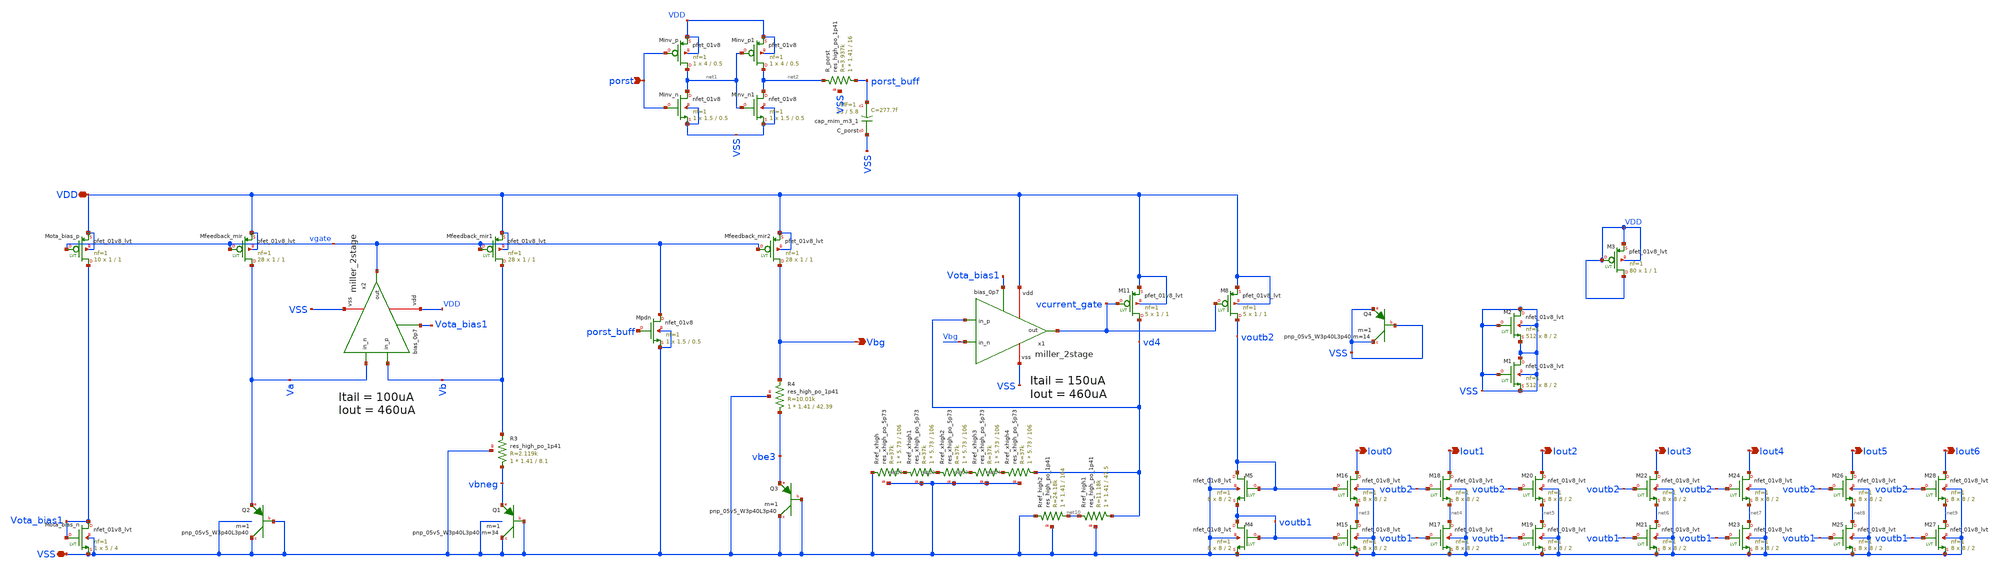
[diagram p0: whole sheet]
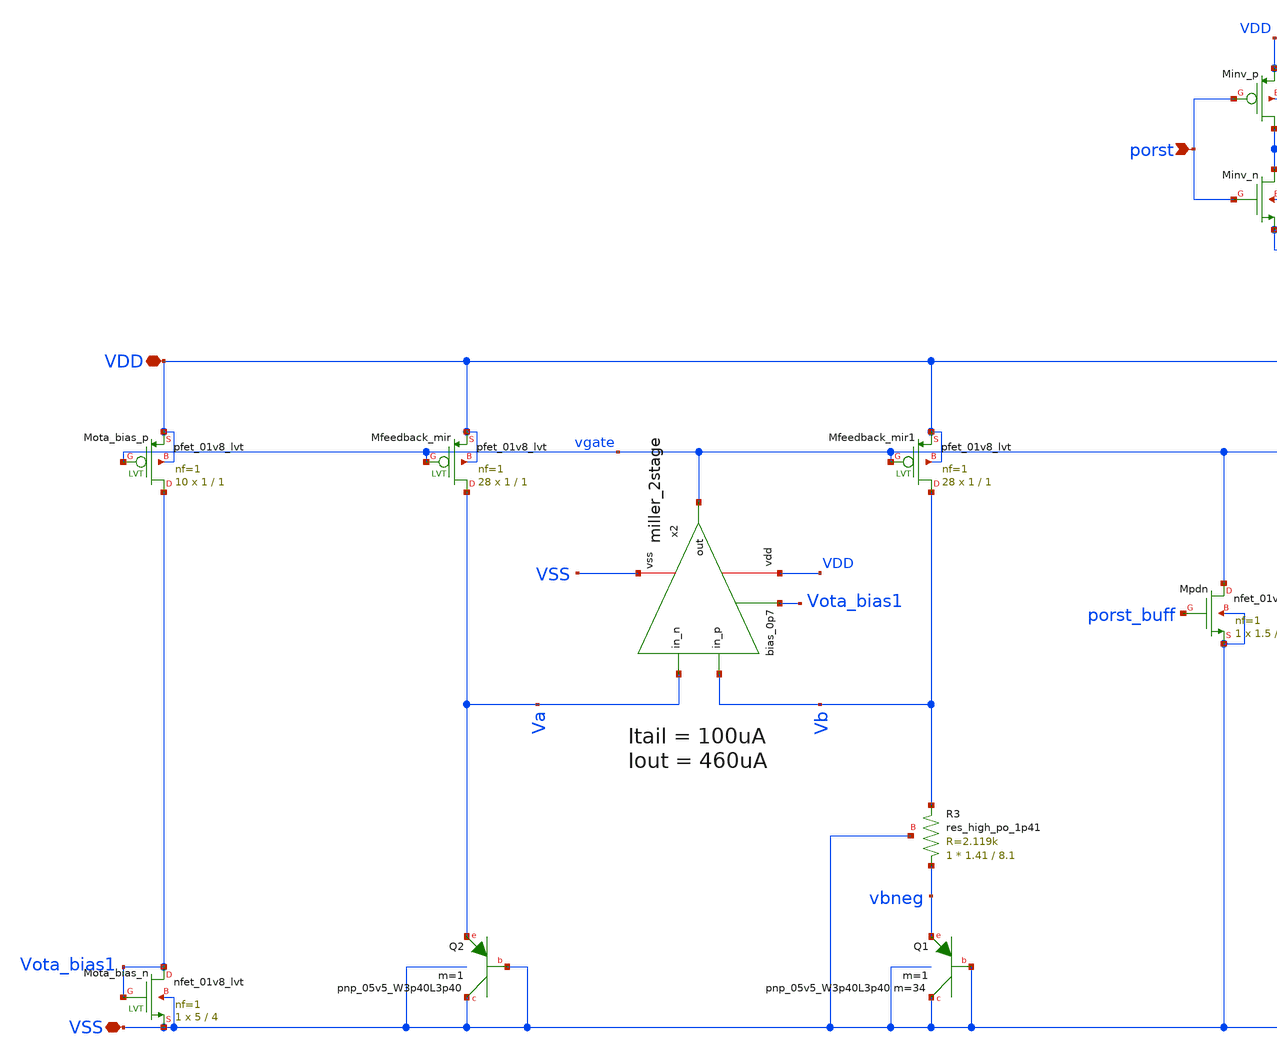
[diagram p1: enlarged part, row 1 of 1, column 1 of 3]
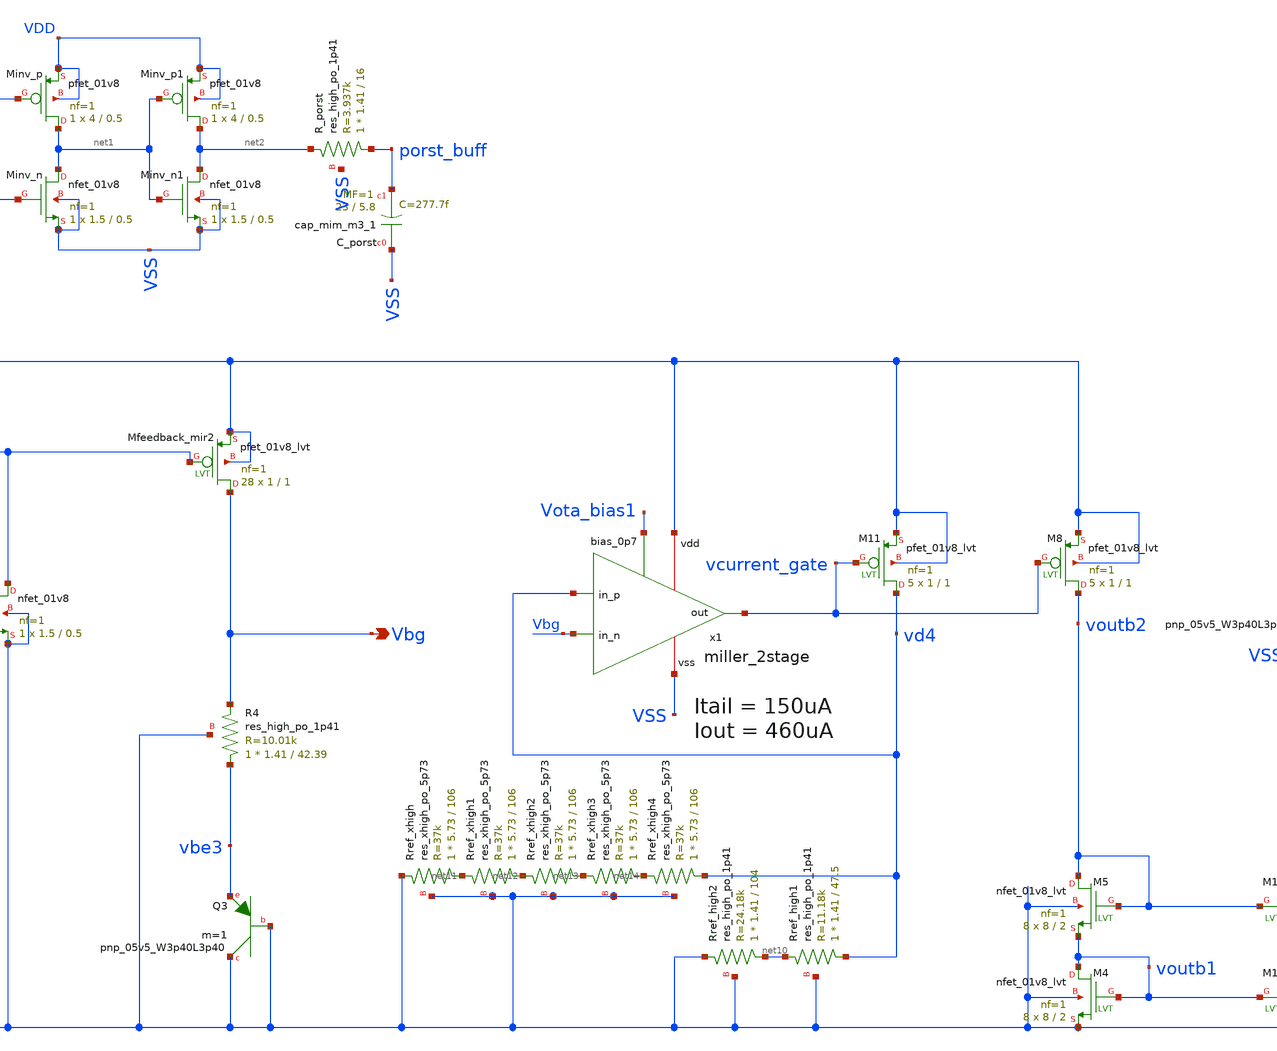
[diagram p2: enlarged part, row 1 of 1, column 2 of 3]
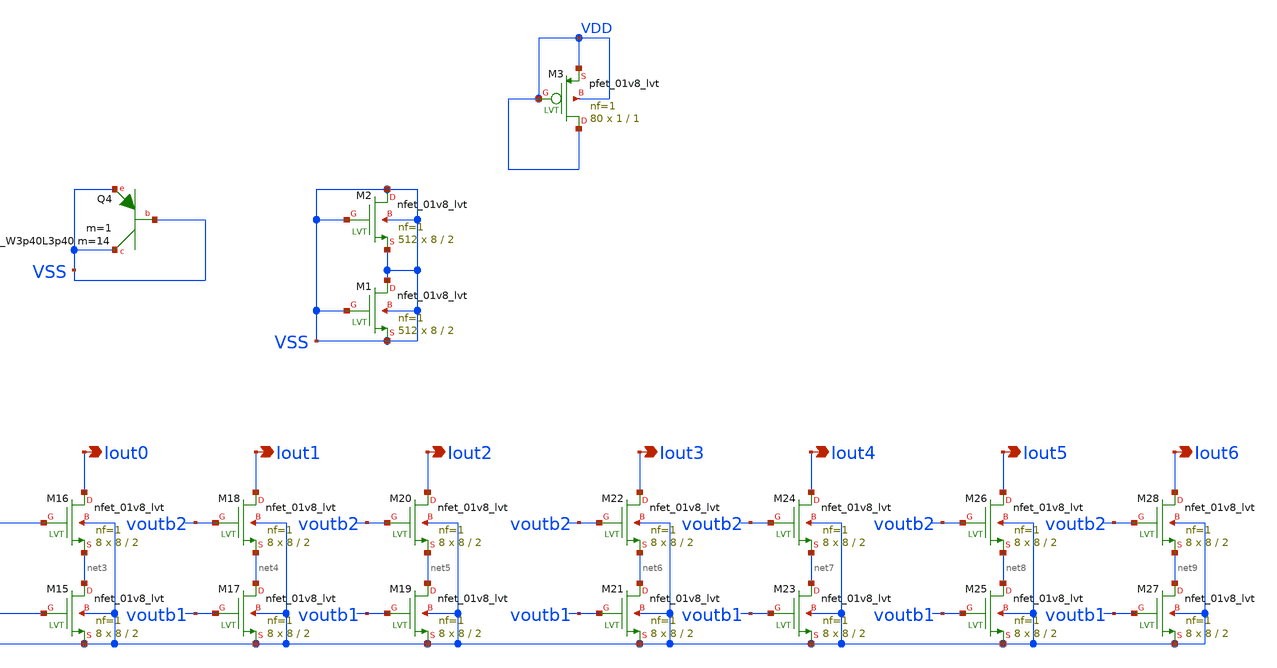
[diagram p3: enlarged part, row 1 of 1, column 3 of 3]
** sch_path: xschem/current_reference/BGR_lvs.sch
**.subckt BGR_lvs Iout0 VDD VSS Iout1 Iout2 porst Vbg Iout3 Iout4 Iout5 Iout6
*.opin Iout0
*.iopin VDD
*.iopin VSS
*.opin Iout1
*.opin Iout2
*.ipin porst
*.opin Vbg
*.opin Iout3
*.opin Iout4
*.opin Iout5
*.opin Iout6
XQ2 VSS VSS Va sky130_fd_pr__pnp_05v5_W3p40L3p40 m=1
XQ1 VSS VSS vbneg sky130_fd_pr__pnp_05v5_W3p40L3p40 m=34 m=1
XMota_bias_n Vota_bias1 Vota_bias1 VSS VSS sky130_fd_pr__nfet_01v8_lvt L=4 W=5 nf=1 ad='int((nf+1)/2) * W/nf * 0.29'
+ as='int((nf+2)/2) * W/nf * 0.29' pd='2*int((nf+1)/2) * (W/nf + 0.29)' ps='2*int((nf+2)/2) * (W/nf + 0.29)'
+ nrd='0.29 / W' nrs='0.29 / W' sa=0 sb=0 sd=0 mult=1 m=1
XMota_bias_p Vota_bias1 vgate VDD VDD sky130_fd_pr__pfet_01v8_lvt L=1 W=1 nf=1 ad='int((nf+1)/2) * W/nf * 0.29'
+ as='int((nf+2)/2) * W/nf * 0.29' pd='2*int((nf+1)/2) * (W/nf + 0.29)' ps='2*int((nf+2)/2) * (W/nf + 0.29)'
+ nrd='0.29 / W' nrs='0.29 / W' sa=0 sb=0 sd=0 mult=10 m=10
XMfeedback_mir Va vgate VDD VDD sky130_fd_pr__pfet_01v8_lvt L=1 W=1 nf=1 ad='int((nf+1)/2) * W/nf * 0.29'
+ as='int((nf+2)/2) * W/nf * 0.29' pd='2*int((nf+1)/2) * (W/nf + 0.29)' ps='2*int((nf+2)/2) * (W/nf + 0.29)'
+ nrd='0.29 / W' nrs='0.29 / W' sa=0 sb=0 sd=0 mult=28 m=28
XMfeedback_mir1 Vb vgate VDD VDD sky130_fd_pr__pfet_01v8_lvt L=1 W=1 nf=1 ad='int((nf+1)/2) * W/nf * 0.29'
+ as='int((nf+2)/2) * W/nf * 0.29' pd='2*int((nf+1)/2) * (W/nf + 0.29)' ps='2*int((nf+2)/2) * (W/nf + 0.29)'
+ nrd='0.29 / W' nrs='0.29 / W' sa=0 sb=0 sd=0 mult=28 m=28
XMfeedback_mir2 Vbg vgate VDD VDD sky130_fd_pr__pfet_01v8_lvt L=1 W=1 nf=1 ad='int((nf+1)/2) * W/nf * 0.29'
+ as='int((nf+2)/2) * W/nf * 0.29' pd='2*int((nf+1)/2) * (W/nf + 0.29)' ps='2*int((nf+2)/2) * (W/nf + 0.29)'
+ nrd='0.29 / W' nrs='0.29 / W' sa=0 sb=0 sd=0 mult=28 m=28
XQ3 VSS VSS vbe3 sky130_fd_pr__pnp_05v5_W3p40L3p40 m=1
XM11 vd4 vcurrent_gate VDD VDD sky130_fd_pr__pfet_01v8_lvt L=1 W=1 nf=1 ad='int((nf+1)/2) * W/nf * 0.29'
+ as='int((nf+2)/2) * W/nf * 0.29' pd='2*int((nf+1)/2) * (W/nf + 0.29)' ps='2*int((nf+2)/2) * (W/nf + 0.29)'
+ nrd='0.29 / W' nrs='0.29 / W' sa=0 sb=0 sd=0 mult=5 m=5
XM8 voutb2 vcurrent_gate VDD VDD sky130_fd_pr__pfet_01v8_lvt L=1 W=1 nf=1 ad='int((nf+1)/2) * W/nf * 0.29'
+ as='int((nf+2)/2) * W/nf * 0.29' pd='2*int((nf+1)/2) * (W/nf + 0.29)' ps='2*int((nf+2)/2) * (W/nf + 0.29)'
+ nrd='0.29 / W' nrs='0.29 / W' sa=0 sb=0 sd=0 mult=5 m=5
XM4 voutb1 voutb1 VSS VSS sky130_fd_pr__nfet_01v8_lvt L=2 W=8 nf=1 ad='int((nf+1)/2) * W/nf * 0.29' as='int((nf+2)/2) * W/nf * 0.29'
+ pd='2*int((nf+1)/2) * (W/nf + 0.29)' ps='2*int((nf+2)/2) * (W/nf + 0.29)' nrd='0.29 / W' nrs='0.29 / W'
+ sa=0 sb=0 sd=0 mult=8 m=8
XM5 voutb2 voutb2 voutb1 VSS sky130_fd_pr__nfet_01v8_lvt L=2 W=8 nf=1 ad='int((nf+1)/2) * W/nf * 0.29'
+ as='int((nf+2)/2) * W/nf * 0.29' pd='2*int((nf+1)/2) * (W/nf + 0.29)' ps='2*int((nf+2)/2) * (W/nf + 0.29)'
+ nrd='0.29 / W' nrs='0.29 / W' sa=0 sb=0 sd=0 mult=8 m=8
XMinv_n net1 porst VSS VSS sky130_fd_pr__nfet_01v8 L=0.5 W=1.5 nf=1 ad='int((nf+1)/2) * W/nf * 0.29'
+ as='int((nf+2)/2) * W/nf * 0.29' pd='2*int((nf+1)/2) * (W/nf + 0.29)' ps='2*int((nf+2)/2) * (W/nf + 0.29)'
+ nrd='0.29 / W' nrs='0.29 / W' sa=0 sb=0 sd=0 mult=1 m=1
XMinv_p net1 porst VDD VDD sky130_fd_pr__pfet_01v8 L=0.5 W=4 nf=1 ad='int((nf+1)/2) * W/nf * 0.29' as='int((nf+2)/2) * W/nf * 0.29'
+ pd='2*int((nf+1)/2) * (W/nf + 0.29)' ps='2*int((nf+2)/2) * (W/nf + 0.29)' nrd='0.29 / W' nrs='0.29 / W'
+ sa=0 sb=0 sd=0 mult=1 m=1
XMinv_n1 net2 net1 VSS VSS sky130_fd_pr__nfet_01v8 L=0.5 W=1.5 nf=1 ad='int((nf+1)/2) * W/nf * 0.29'
+ as='int((nf+2)/2) * W/nf * 0.29' pd='2*int((nf+1)/2) * (W/nf + 0.29)' ps='2*int((nf+2)/2) * (W/nf + 0.29)'
+ nrd='0.29 / W' nrs='0.29 / W' sa=0 sb=0 sd=0 mult=1 m=1
XMinv_p1 net2 net1 VDD VDD sky130_fd_pr__pfet_01v8 L=0.5 W=4 nf=1 ad='int((nf+1)/2) * W/nf * 0.29' as='int((nf+2)/2) * W/nf * 0.29'
+ pd='2*int((nf+1)/2) * (W/nf + 0.29)' ps='2*int((nf+2)/2) * (W/nf + 0.29)' nrd='0.29 / W' nrs='0.29 / W'
+ sa=0 sb=0 sd=0 mult=1 m=1
XM15 net3 voutb1 VSS VSS sky130_fd_pr__nfet_01v8_lvt L=2 W=8 nf=1 ad='int((nf+1)/2) * W/nf * 0.29' as='int((nf+2)/2) * W/nf * 0.29'
+ pd='2*int((nf+1)/2) * (W/nf + 0.29)' ps='2*int((nf+2)/2) * (W/nf + 0.29)' nrd='0.29 / W' nrs='0.29 / W'
+ sa=0 sb=0 sd=0 mult=8 m=8
XM16 Iout0 voutb2 net3 VSS sky130_fd_pr__nfet_01v8_lvt L=2 W=8 nf=1 ad='int((nf+1)/2) * W/nf * 0.29'
+ as='int((nf+2)/2) * W/nf * 0.29' pd='2*int((nf+1)/2) * (W/nf + 0.29)' ps='2*int((nf+2)/2) * (W/nf + 0.29)'
+ nrd='0.29 / W' nrs='0.29 / W' sa=0 sb=0 sd=0 mult=8 m=8
XM17 net4 voutb1 VSS VSS sky130_fd_pr__nfet_01v8_lvt L=2 W=8 nf=1 ad='int((nf+1)/2) * W/nf * 0.29' as='int((nf+2)/2) * W/nf * 0.29'
+ pd='2*int((nf+1)/2) * (W/nf + 0.29)' ps='2*int((nf+2)/2) * (W/nf + 0.29)' nrd='0.29 / W' nrs='0.29 / W'
+ sa=0 sb=0 sd=0 mult=8 m=8
XM18 Iout1 voutb2 net4 VSS sky130_fd_pr__nfet_01v8_lvt L=2 W=8 nf=1 ad='int((nf+1)/2) * W/nf * 0.29'
+ as='int((nf+2)/2) * W/nf * 0.29' pd='2*int((nf+1)/2) * (W/nf + 0.29)' ps='2*int((nf+2)/2) * (W/nf + 0.29)'
+ nrd='0.29 / W' nrs='0.29 / W' sa=0 sb=0 sd=0 mult=8 m=8
XC_porst VSS porst_buff sky130_fd_pr__cap_mim_m3_1 W=23 L=5.8 MF=1 m=1
XM19 net5 voutb1 VSS VSS sky130_fd_pr__nfet_01v8_lvt L=2 W=8 nf=1 ad='int((nf+1)/2) * W/nf * 0.29' as='int((nf+2)/2) * W/nf * 0.29'
+ pd='2*int((nf+1)/2) * (W/nf + 0.29)' ps='2*int((nf+2)/2) * (W/nf + 0.29)' nrd='0.29 / W' nrs='0.29 / W'
+ sa=0 sb=0 sd=0 mult=8 m=8
XM20 Iout2 voutb2 net5 VSS sky130_fd_pr__nfet_01v8_lvt L=2 W=8 nf=1 ad='int((nf+1)/2) * W/nf * 0.29'
+ as='int((nf+2)/2) * W/nf * 0.29' pd='2*int((nf+1)/2) * (W/nf + 0.29)' ps='2*int((nf+2)/2) * (W/nf + 0.29)'
+ nrd='0.29 / W' nrs='0.29 / W' sa=0 sb=0 sd=0 mult=8 m=8
XM21 net6 voutb1 VSS VSS sky130_fd_pr__nfet_01v8_lvt L=2 W=8 nf=1 ad='int((nf+1)/2) * W/nf * 0.29' as='int((nf+2)/2) * W/nf * 0.29'
+ pd='2*int((nf+1)/2) * (W/nf + 0.29)' ps='2*int((nf+2)/2) * (W/nf + 0.29)' nrd='0.29 / W' nrs='0.29 / W'
+ sa=0 sb=0 sd=0 mult=8 m=8
XM22 Iout3 voutb2 net6 VSS sky130_fd_pr__nfet_01v8_lvt L=2 W=8 nf=1 ad='int((nf+1)/2) * W/nf * 0.29'
+ as='int((nf+2)/2) * W/nf * 0.29' pd='2*int((nf+1)/2) * (W/nf + 0.29)' ps='2*int((nf+2)/2) * (W/nf + 0.29)'
+ nrd='0.29 / W' nrs='0.29 / W' sa=0 sb=0 sd=0 mult=8 m=8
XM23 net7 voutb1 VSS VSS sky130_fd_pr__nfet_01v8_lvt L=2 W=8 nf=1 ad='int((nf+1)/2) * W/nf * 0.29' as='int((nf+2)/2) * W/nf * 0.29'
+ pd='2*int((nf+1)/2) * (W/nf + 0.29)' ps='2*int((nf+2)/2) * (W/nf + 0.29)' nrd='0.29 / W' nrs='0.29 / W'
+ sa=0 sb=0 sd=0 mult=8 m=8
XM24 Iout4 voutb2 net7 VSS sky130_fd_pr__nfet_01v8_lvt L=2 W=8 nf=1 ad='int((nf+1)/2) * W/nf * 0.29'
+ as='int((nf+2)/2) * W/nf * 0.29' pd='2*int((nf+1)/2) * (W/nf + 0.29)' ps='2*int((nf+2)/2) * (W/nf + 0.29)'
+ nrd='0.29 / W' nrs='0.29 / W' sa=0 sb=0 sd=0 mult=8 m=8
XM25 net8 voutb1 VSS VSS sky130_fd_pr__nfet_01v8_lvt L=2 W=8 nf=1 ad='int((nf+1)/2) * W/nf * 0.29' as='int((nf+2)/2) * W/nf * 0.29'
+ pd='2*int((nf+1)/2) * (W/nf + 0.29)' ps='2*int((nf+2)/2) * (W/nf + 0.29)' nrd='0.29 / W' nrs='0.29 / W'
+ sa=0 sb=0 sd=0 mult=8 m=8
XM26 Iout5 voutb2 net8 VSS sky130_fd_pr__nfet_01v8_lvt L=2 W=8 nf=1 ad='int((nf+1)/2) * W/nf * 0.29'
+ as='int((nf+2)/2) * W/nf * 0.29' pd='2*int((nf+1)/2) * (W/nf + 0.29)' ps='2*int((nf+2)/2) * (W/nf + 0.29)'
+ nrd='0.29 / W' nrs='0.29 / W' sa=0 sb=0 sd=0 mult=8 m=8
XM27 net9 voutb1 VSS VSS sky130_fd_pr__nfet_01v8_lvt L=2 W=8 nf=1 ad='int((nf+1)/2) * W/nf * 0.29' as='int((nf+2)/2) * W/nf * 0.29'
+ pd='2*int((nf+1)/2) * (W/nf + 0.29)' ps='2*int((nf+2)/2) * (W/nf + 0.29)' nrd='0.29 / W' nrs='0.29 / W'
+ sa=0 sb=0 sd=0 mult=8 m=8
XM28 Iout6 voutb2 net9 VSS sky130_fd_pr__nfet_01v8_lvt L=2 W=8 nf=1 ad='int((nf+1)/2) * W/nf * 0.29'
+ as='int((nf+2)/2) * W/nf * 0.29' pd='2*int((nf+1)/2) * (W/nf + 0.29)' ps='2*int((nf+2)/2) * (W/nf + 0.29)'
+ nrd='0.29 / W' nrs='0.29 / W' sa=0 sb=0 sd=0 mult=8 m=8
XRref_xhigh net11 VSS VSS sky130_fd_pr__res_xhigh_po_5p73 L=106 mult=1 m=1
XRref_xhigh1 net12 net11 VSS sky130_fd_pr__res_xhigh_po_5p73 L=106 mult=1 m=1
XRref_xhigh2 net13 net12 VSS sky130_fd_pr__res_xhigh_po_5p73 L=106 mult=1 m=1
XRref_xhigh3 net14 net13 VSS sky130_fd_pr__res_xhigh_po_5p73 L=106 mult=1 m=1
XRref_xhigh4 vd4 net14 VSS sky130_fd_pr__res_xhigh_po_5p73 L=106 mult=1 m=1
XR4 vbe3 Vbg VSS sky130_fd_pr__res_high_po_1p41 L=42.39 mult=1 m=1
XR3 vbneg Vb VSS sky130_fd_pr__res_high_po_1p41 L=8.1 mult=1 m=1
XR_porst porst_buff net2 VSS sky130_fd_pr__res_high_po_1p41 L=16 mult=1 m=1
XRref_high1 vd4 net10 VSS sky130_fd_pr__res_high_po_1p41 L=47.5 mult=1 m=1
XRref_high2 net10 VSS VSS sky130_fd_pr__res_high_po_1p41 L=104 mult=1 m=1
XM1 VSS VSS VSS VSS sky130_fd_pr__nfet_01v8_lvt L=2 W=8 nf=1 ad='int((nf+1)/2) * W/nf * 0.29' as='int((nf+2)/2) * W/nf * 0.29'
+ pd='2*int((nf+1)/2) * (W/nf + 0.29)' ps='2*int((nf+2)/2) * (W/nf + 0.29)' nrd='0.29 / W' nrs='0.29 / W'
+ sa=0 sb=0 sd=0 mult=512 m=512
XM2 VSS VSS VSS VSS sky130_fd_pr__nfet_01v8_lvt L=2 W=8 nf=1 ad='int((nf+1)/2) * W/nf * 0.29' as='int((nf+2)/2) * W/nf * 0.29'
+ pd='2*int((nf+1)/2) * (W/nf + 0.29)' ps='2*int((nf+2)/2) * (W/nf + 0.29)' nrd='0.29 / W' nrs='0.29 / W'
+ sa=0 sb=0 sd=0 mult=512 m=512
XM3 VDD VDD VDD VDD sky130_fd_pr__pfet_01v8_lvt L=1 W=1 nf=1 ad='int((nf+1)/2) * W/nf * 0.29' as='int((nf+2)/2) * W/nf * 0.29'
+ pd='2*int((nf+1)/2) * (W/nf + 0.29)' ps='2*int((nf+2)/2) * (W/nf + 0.29)' nrd='0.29 / W' nrs='0.29 / W'
+ sa=0 sb=0 sd=0 mult=80 m=80
XMpdn vgate porst_buff VSS VSS sky130_fd_pr__nfet_01v8 L=0.5 W=1.5 nf=1 ad='int((nf+1)/2) * W/nf * 0.29'
+ as='int((nf+2)/2) * W/nf * 0.29' pd='2*int((nf+1)/2) * (W/nf + 0.29)' ps='2*int((nf+2)/2) * (W/nf + 0.29)'
+ nrd='0.29 / W' nrs='0.29 / W' sa=0 sb=0 sd=0 mult=1 m=1
XQ4 VSS VSS VSS sky130_fd_pr__pnp_05v5_W3p40L3p40 m=14 m=1
x1 VDD Vbg vd4 vcurrent_gate Vota_bias1 VSS miller_2stage
x2 VDD Va Vb vgate Vota_bias1 VSS miller_2stage
**.ends
.end
